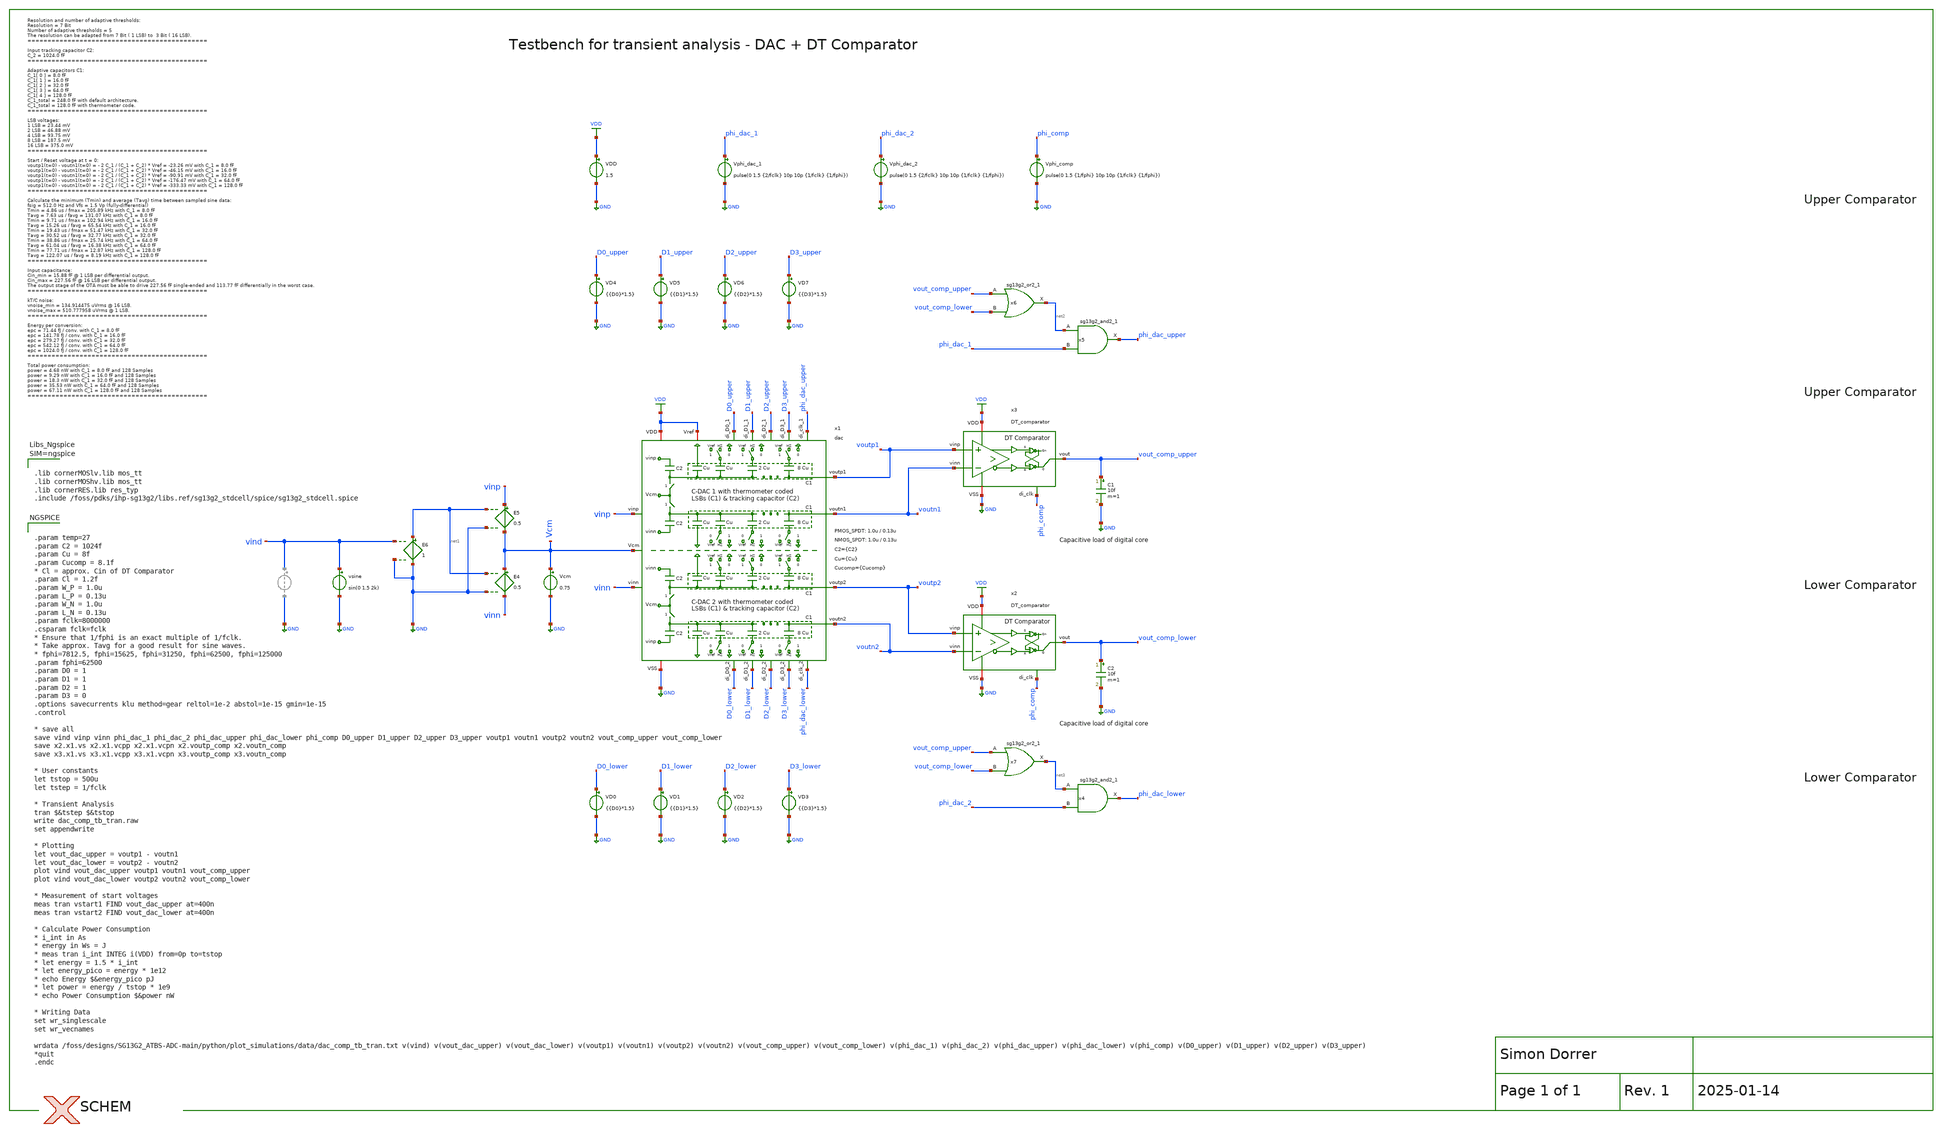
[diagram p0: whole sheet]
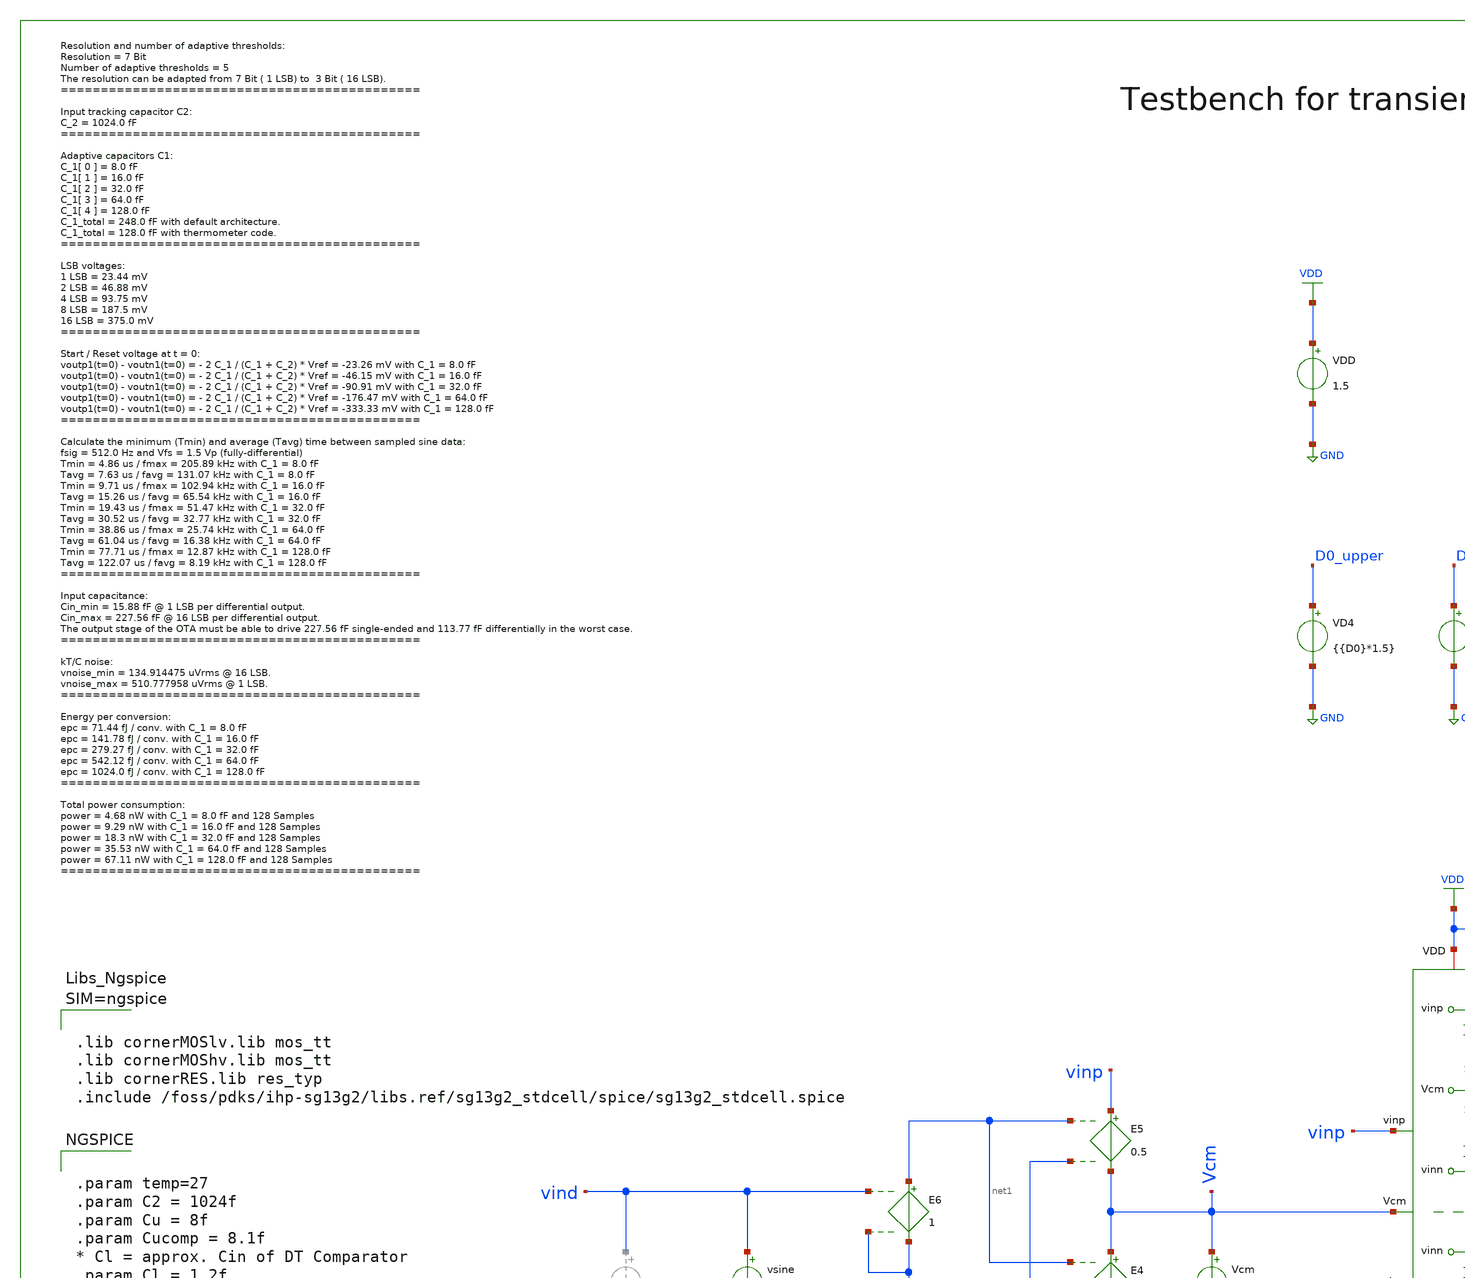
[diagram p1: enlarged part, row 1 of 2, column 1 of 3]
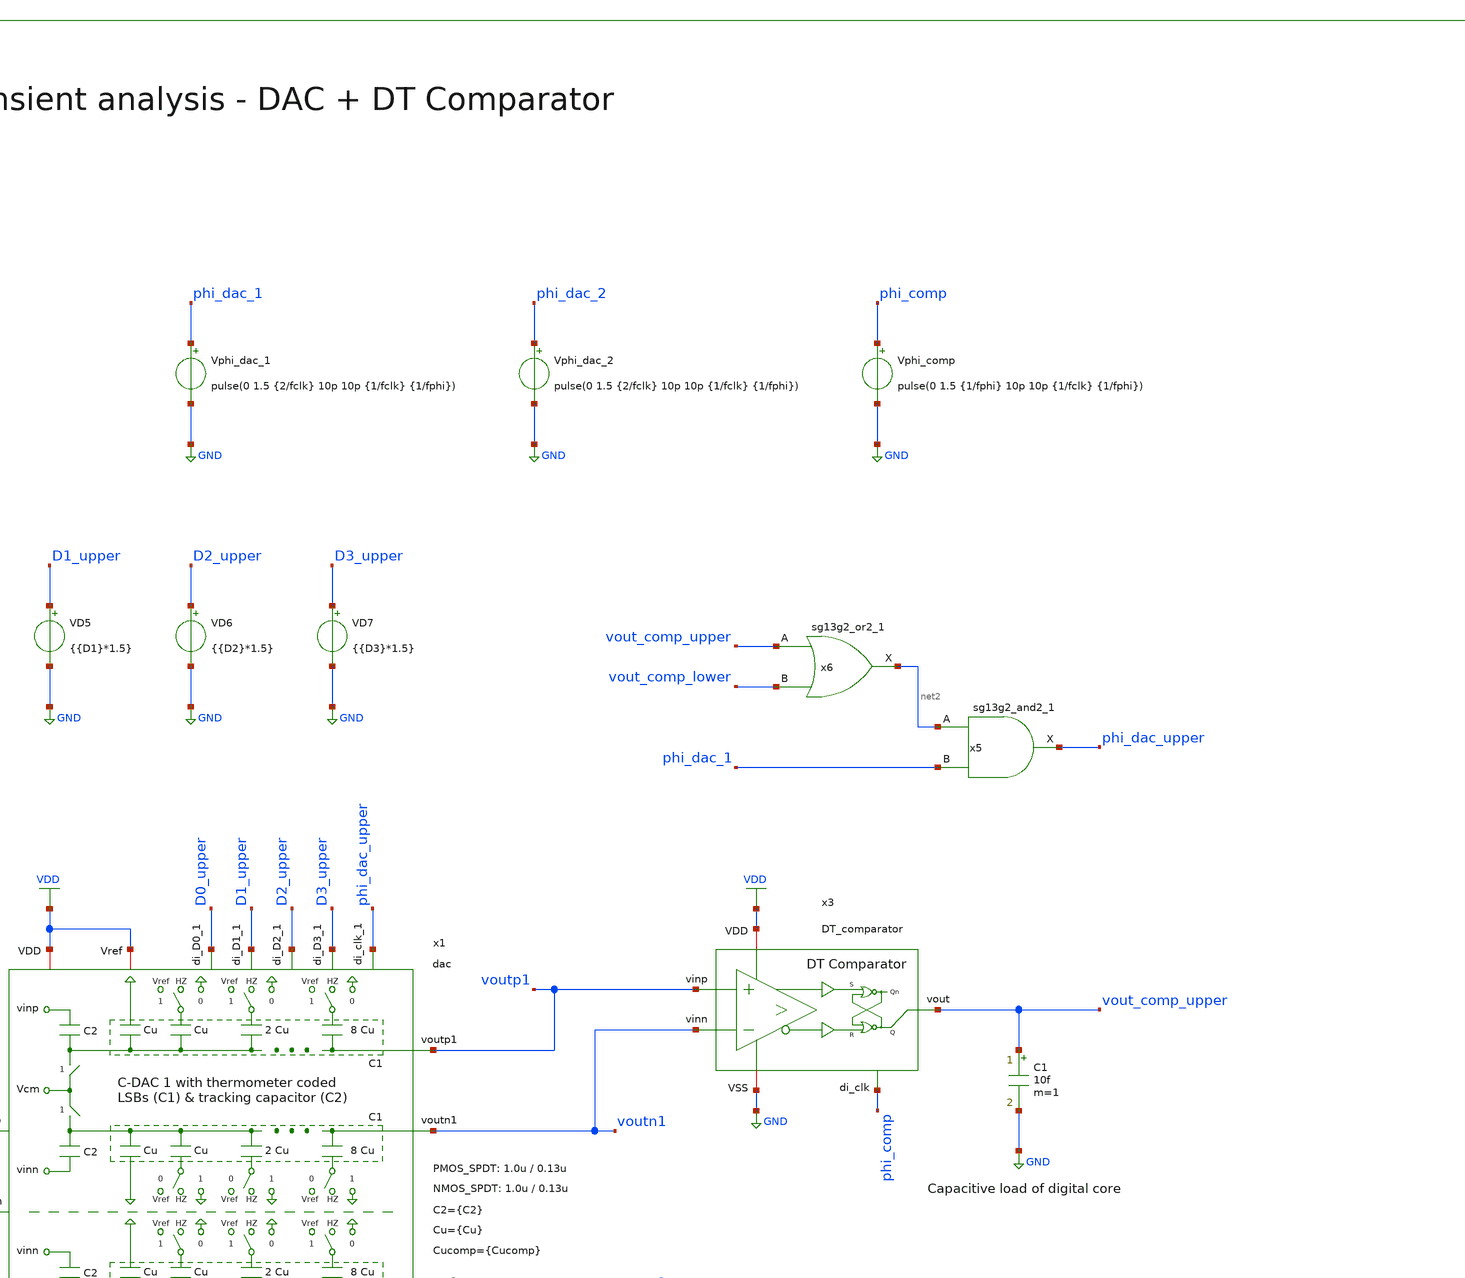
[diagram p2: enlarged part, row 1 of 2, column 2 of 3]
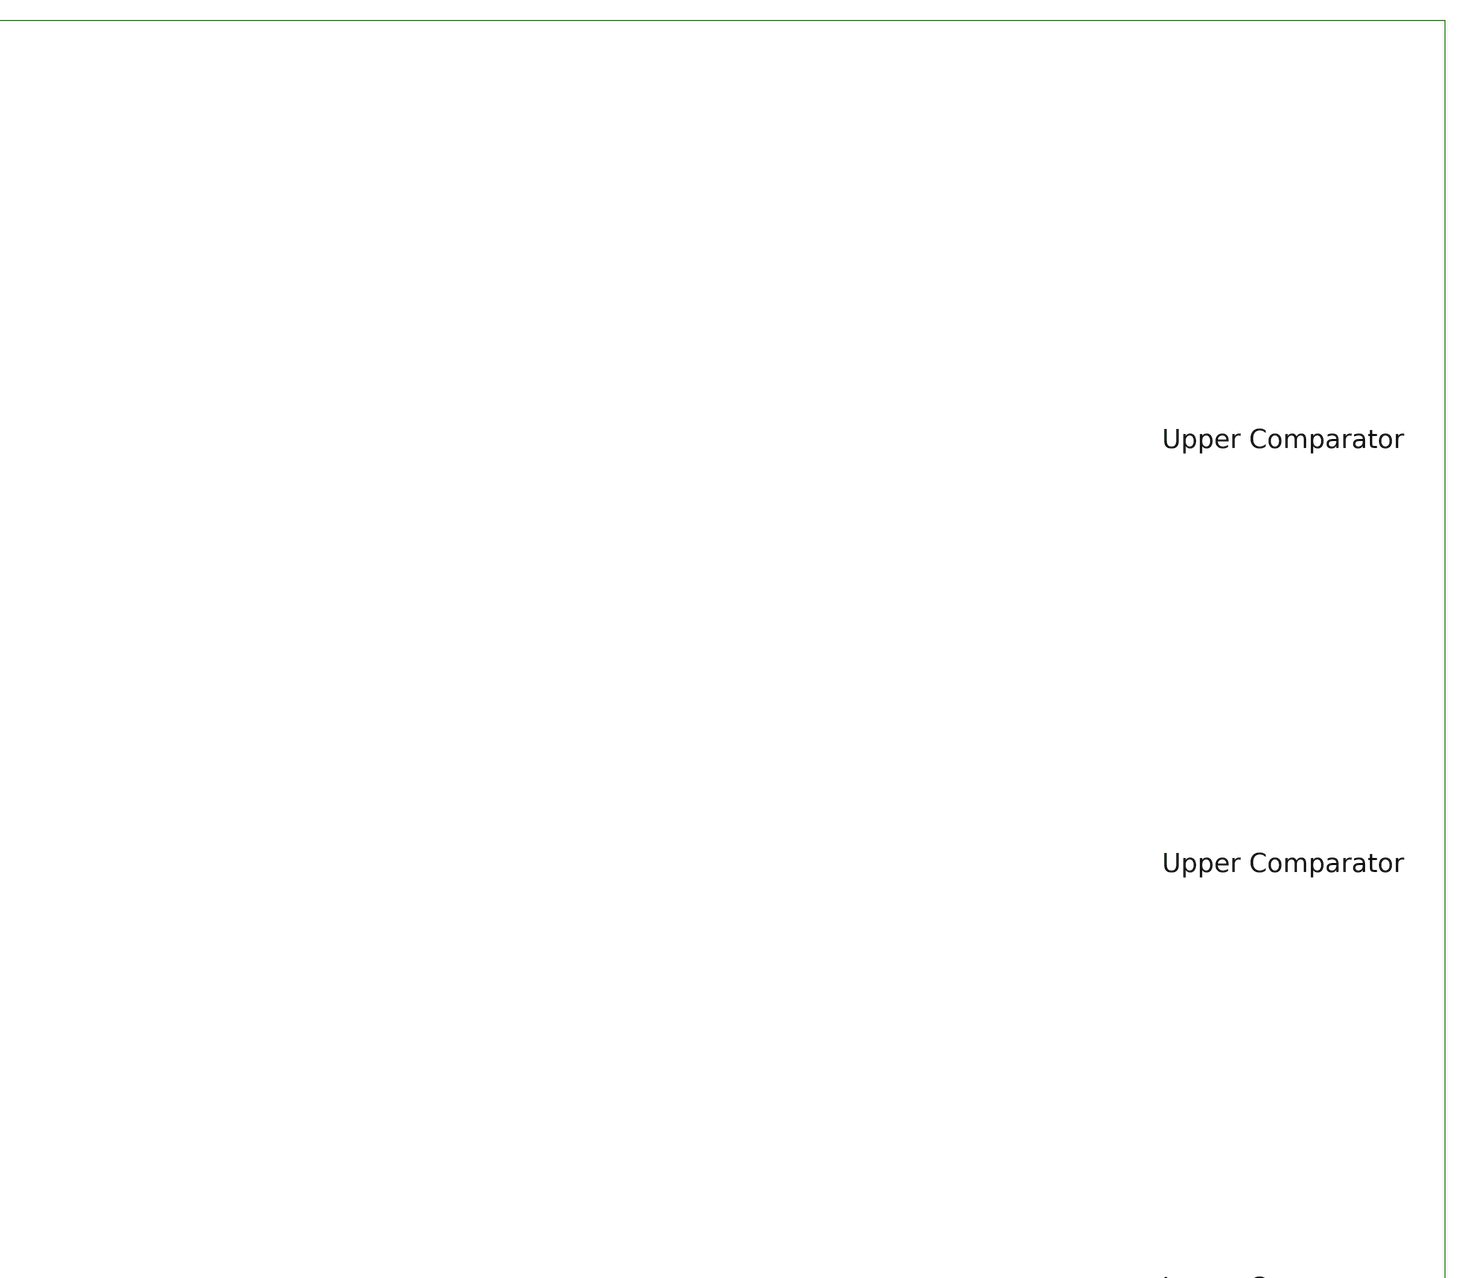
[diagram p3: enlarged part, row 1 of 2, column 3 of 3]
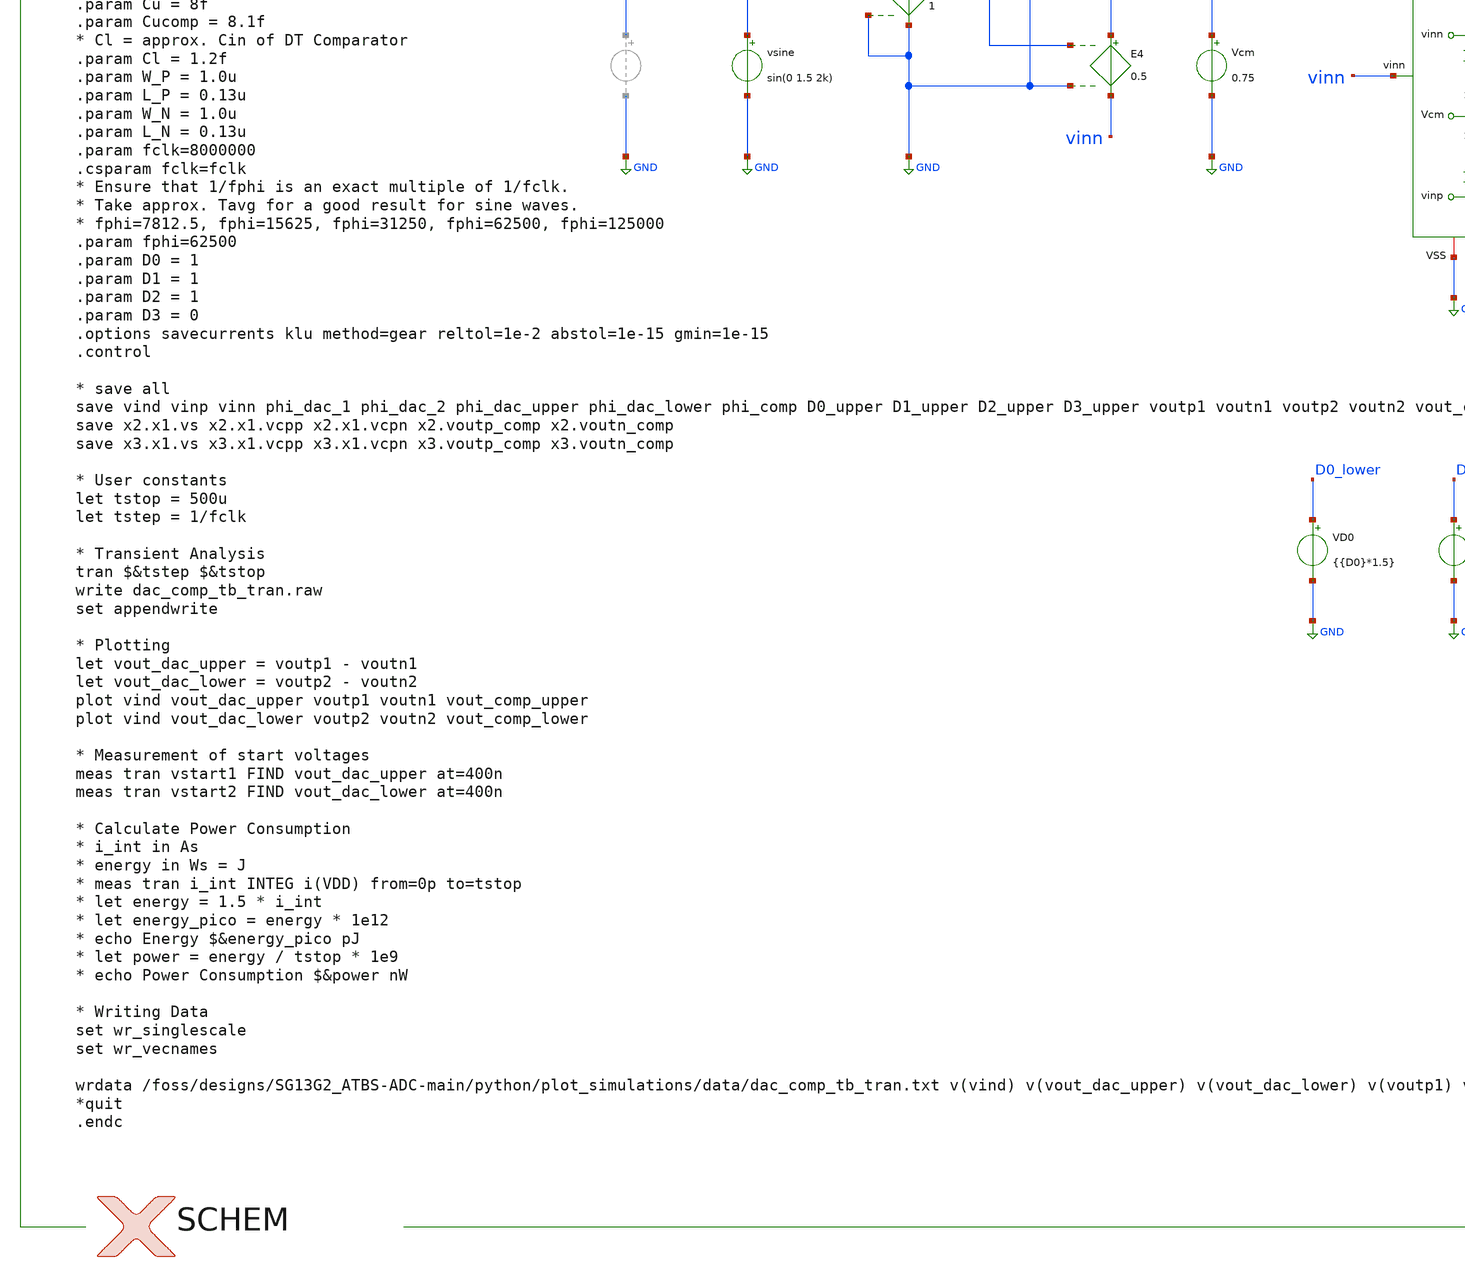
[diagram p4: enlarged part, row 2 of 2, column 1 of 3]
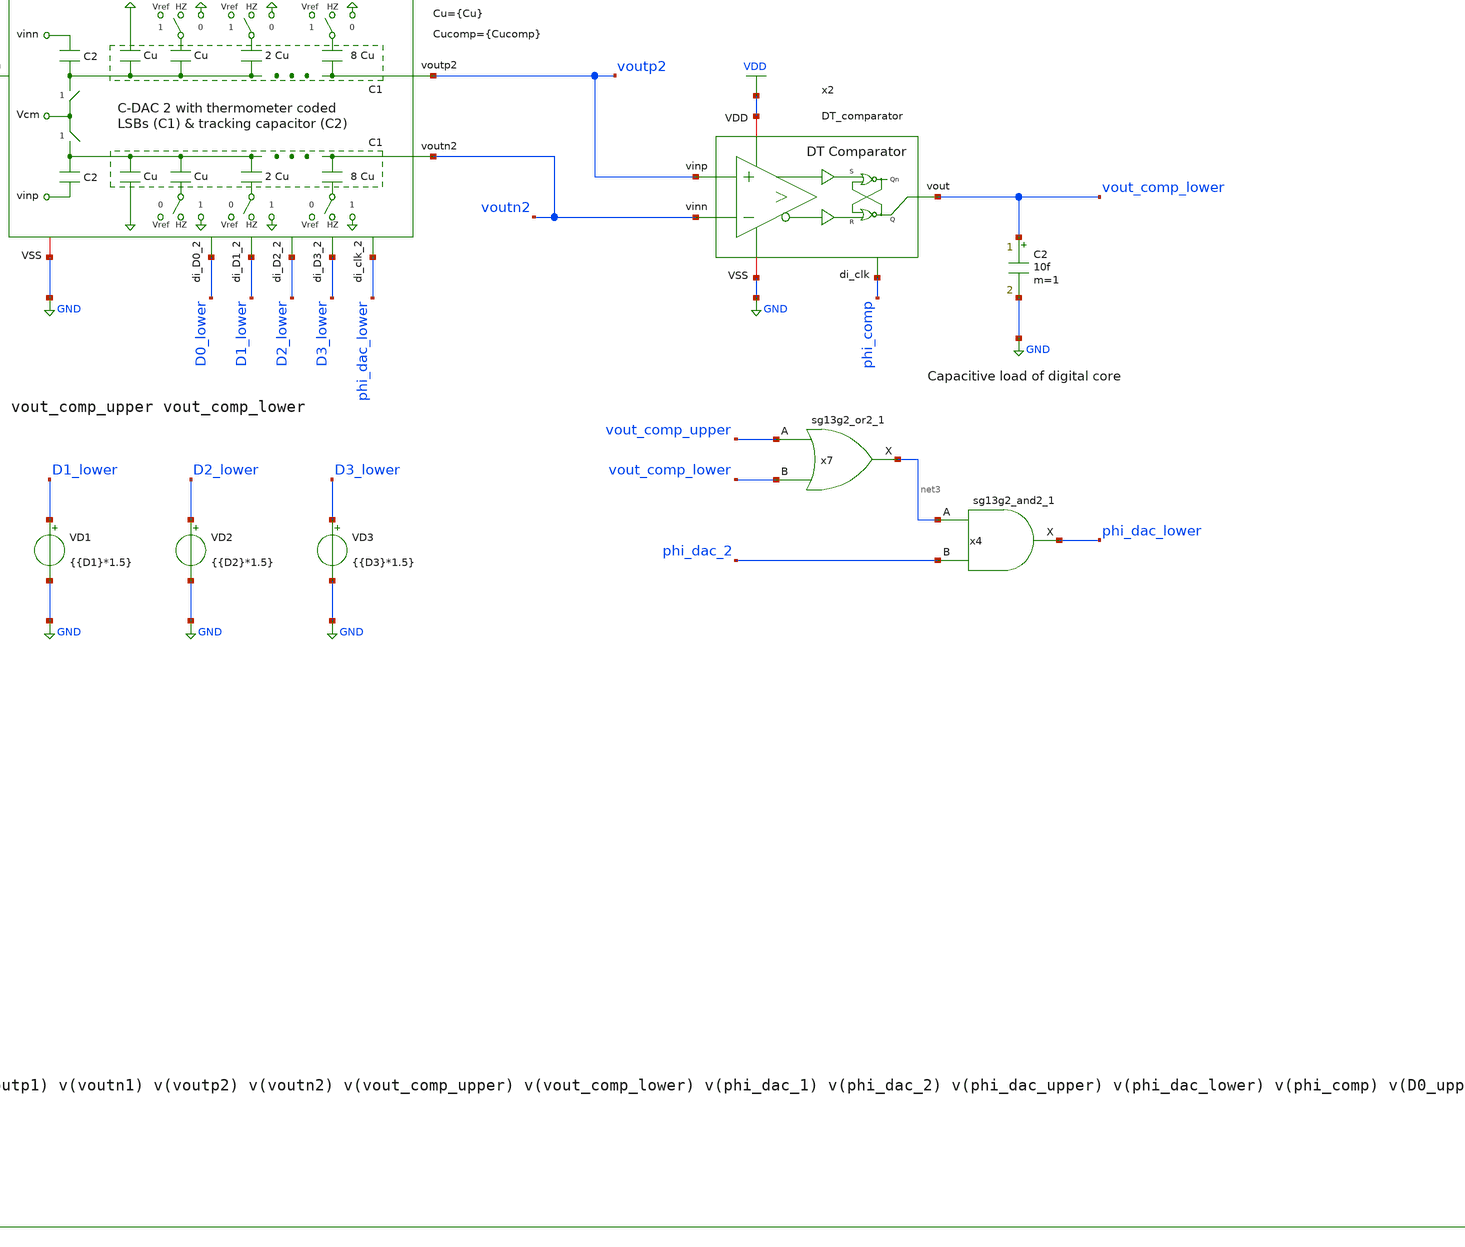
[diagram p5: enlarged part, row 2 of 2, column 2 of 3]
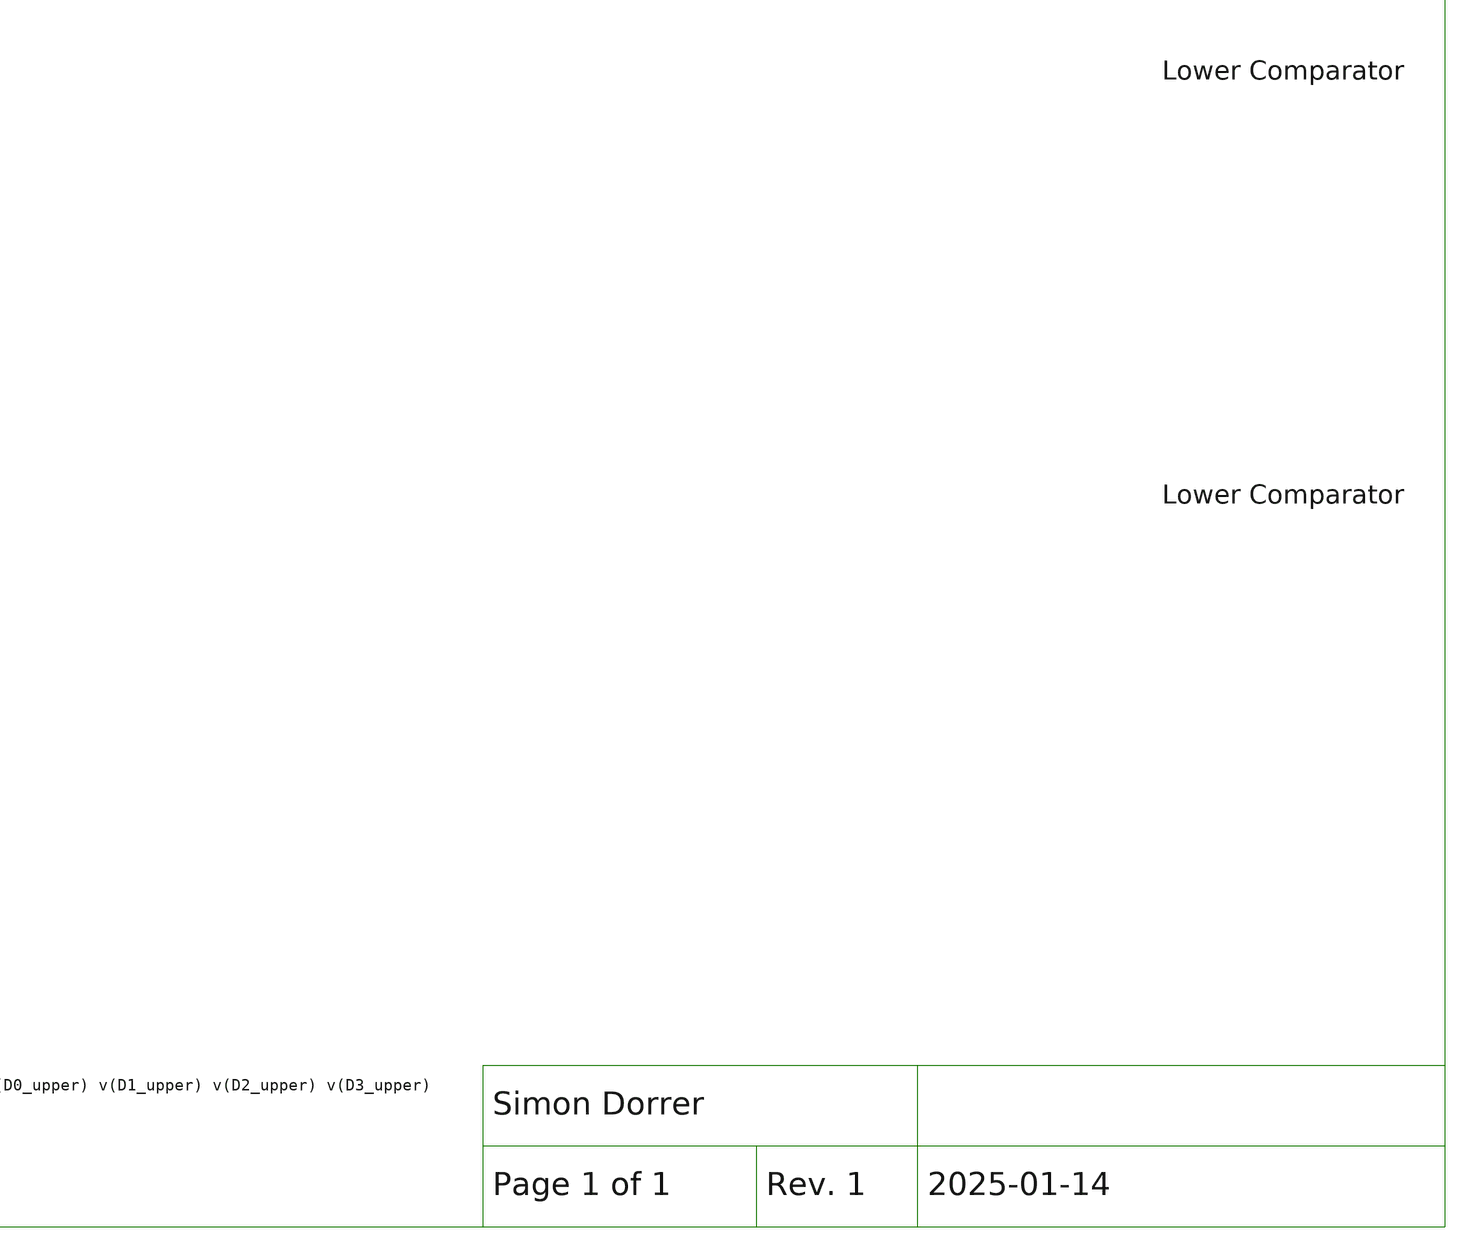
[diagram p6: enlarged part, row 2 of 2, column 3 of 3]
** sch_path: SG13G2_ATBS-ADC-main/xschem/dac/testbenches/dac_comp_tb_tran.sch
**.subckt dac_comp_tb_tran
VDD VDD GND 1.5
Vcm Vcm GND 0.75
E4 Vcm vinn net1 GND 0.5
E5 vinp Vcm net1 GND 0.5
E6 net1 GND vind GND 1
VD0 D0_lower GND {{D0}*1.5}
VD1 D1_lower GND {{D1}*1.5}
VD2 D2_lower GND {{D2}*1.5}
VD3 D3_lower GND {{D3}*1.5}
Vphi_comp phi_comp GND pulse(0 1.5 {1/fphi} 10p 10p {1/fclk} {1/fphi})
Vphi_dac_1 phi_dac_1 GND pulse(0 1.5 {2/fclk} 10p 10p {1/fclk} {1/fphi})
x2 VDD voutp2 vout_comp_lower voutn2 phi_comp GND DT_comparator
x3 VDD voutp1 vout_comp_upper voutn1 phi_comp GND DT_comparator
vsine vind GND sin(0 1.5 2k)
x1 VDD vinp voutp1 voutn1 vinn D0_lower D1_lower D2_lower D3_lower GND VDD Vcm voutp2 voutn2 phi_dac_lower
+ D0_upper D1_upper D2_upper D3_upper phi_dac_upper dac W_P_SPDT=1.0u L_P_SPDT=0.13u W_N_SPDT=1.0u L_N_SPDT=0.13u
+ C2={C2} Cu={Cu} Cucomp={Cucomp}
C1 vout_comp_upper GND 10f m=1
C2 vout_comp_lower GND 10f m=1
x5 phi_dac_upper net2 phi_dac_1 VDD GND sg13g2_and2_1
VD4 D0_upper GND {{D0}*1.5}
VD5 D1_upper GND {{D1}*1.5}
VD6 D2_upper GND {{D2}*1.5}
VD7 D3_upper GND {{D3}*1.5}
x6 net2 vout_comp_upper vout_comp_lower VDD GND sg13g2_or2_1
x4 phi_dac_lower net3 phi_dac_2 VDD GND sg13g2_and2_1
x7 net3 vout_comp_upper vout_comp_lower VDD GND sg13g2_or2_1
Vphi_dac_2 phi_dac_2 GND pulse(0 1.5 {2/fclk} 10p 10p {1/fclk} {1/fphi})
**** begin user architecture code


.param temp=27
.param C2 = 1024f
.param Cu = 8f
.param Cucomp = 8.1f
* Cl = approx. Cin of DT Comparator
.param Cl = 1.2f
.param W_P = 1.0u
.param L_P = 0.13u
.param W_N = 1.0u
.param L_N = 0.13u
.param fclk=8000000
.csparam fclk=fclk
* Ensure that 1/fphi is an exact multiple of 1/fclk.
* Take approx. Tavg for a good result for sine waves.
* fphi=7812.5, fphi=15625, fphi=31250, fphi=62500, fphi=125000
.param fphi=62500
.param D0 = 1
.param D1 = 1
.param D2 = 1
.param D3 = 0
.options savecurrents klu method=gear reltol=1e-2 abstol=1e-15 gmin=1e-15
.control

* save all
save vind vinp vinn phi_dac_1 phi_dac_2 phi_dac_upper phi_dac_lower phi_comp D0_upper D1_upper
+ D2_upper D3_upper voutp1 voutn1 voutp2 voutn2 vout_comp_upper vout_comp_lower
save x2.x1.vs x2.x1.vcpp x2.x1.vcpn x2.voutp_comp x2.voutn_comp
save x3.x1.vs x3.x1.vcpp x3.x1.vcpn x3.voutp_comp x3.voutn_comp

* User constants
let tstop = 500u
let tstep = 1/fclk

* Transient Analysis
tran $&tstep $&tstop
write dac_comp_tb_tran.raw
set appendwrite

* Plotting
let vout_dac_upper = voutp1 - voutn1
let vout_dac_lower = voutp2 - voutn2
plot vind vout_dac_upper voutp1 voutn1 vout_comp_upper
plot vind vout_dac_lower voutp2 voutn2 vout_comp_lower

* Measurement of start voltages
meas tran vstart1 FIND vout_dac_upper at=400n
meas tran vstart2 FIND vout_dac_lower at=400n

* Calculate Power Consumption
* i_int in As
* energy in Ws = J
* meas tran i_int INTEG i(VDD) from=0p to=tstop
* let energy = 1.5 * i_int
* let energy_pico = energy * 1e12
* echo Energy $&energy_pico pJ
* let power = energy / tstop * 1e9
* echo Power Consumption $&power nW

* Writing Data
set wr_singlescale
set wr_vecnames

wrdata /foss/designs/SG13G2_ATBS-ADC-main/python/plot_simulations/data/dac_comp_tb_tran.txt v(vind)
+ v(vout_dac_upper) v(vout_dac_lower) v(voutp1) v(voutn1) v(voutp2) v(voutn2) v(vout_comp_upper) v(vout_comp_lower)
+ v(phi_dac_1) v(phi_dac_2) v(phi_dac_upper) v(phi_dac_lower) v(phi_comp) v(D0_upper) v(D1_upper) v(D2_upper)
+ v(D3_upper)
*quit
.endc





.lib cornerMOSlv.lib mos_tt
.lib cornerMOShv.lib mos_tt
.lib cornerRES.lib res_typ
.include /foss/pdks/ihp-sg13g2/libs.ref/sg13g2_stdcell/spice/sg13g2_stdcell.spice



**** end user architecture code
**.ends

* expanding   symbol:  comparator/discrete_time/DT_comparator.sym # of pins=6
** sym_path: SG13G2_ATBS-ADC-main/xschem/comparator/discrete_time/DT_comparator.sym
** sch_path: SG13G2_ATBS-ADC-main/xschem/comparator/discrete_time/DT_comparator.sch
.subckt DT_comparator VDD vinp vout vinn di_clk VSS
*.iopin VDD
*.opin vout
*.iopin VSS
*.ipin vinp
*.ipin vinn
*.ipin di_clk
x2 VDD voutp_comp voutp_buf VSS buffer_lv W_P_INV=1.0u L_P_INV=0.13u W_N_INV=1.0u L_N_INV=0.13u
x3 VDD voutn_comp voutn_buf VSS buffer_lv W_P_INV=1.0u L_P_INV=0.13u W_N_INV=1.0u L_N_INV=0.13u
x5 VDD di_clk net1 VSS inverter_lv W_P=1.0u L_P=0.13u W_N=1.0u L_N=0.13u
* noconn #net2
x4 VDD voutp_buf net2 VSS vout voutn_buf SR_latch W_P_SR=1.0u L_P_SR=0.13u W_N_SR=1.0u L_N_SR=0.13u
x1 net1 di_clk VDD voutp_comp vinp VSS voutn_comp vinn dynamic_biasing_comparator
.ends


* expanding   symbol:  dac/dac.sym # of pins=20
** sym_path: SG13G2_ATBS-ADC-main/xschem/dac/dac.sym
** sch_path: SG13G2_ATBS-ADC-main/xschem/dac/dac.sch
.subckt dac VDD vinp voutp1 voutn1 vinn di_D0_2 di_D1_2 di_D2_2 di_D3_2 VSS Vref Vcm voutp2 voutn2
+ di_clk_2 di_D0_1 di_D1_1 di_D2_1 di_D3_1 di_clk_1  W_P_SPDT=1.0u L_P_SPDT=0.13u W_N_SPDT=1.0u L_N_SPDT=0.13u
+ C2=1024f Cu=8f Cucomp=8.1f
*.opin voutp1
*.ipin di_D0_1
*.iopin VSS
*.iopin Vref
*.opin voutn1
*.ipin vinp
*.ipin vinn
*.ipin di_D1_1
*.ipin di_D2_1
*.ipin di_D3_1
*.opin voutp2
*.opin voutn2
*.iopin VDD
*.ipin Vcm
*.ipin di_clk_1
*.ipin di_D3_2
*.ipin di_D2_2
*.ipin di_D1_2
*.ipin di_D0_2
*.ipin di_clk_2
C2a vinp voutp1 C2 m=1
C2b vinn voutn1 C2 m=1
C1a net3 voutp1 Cucomp m=1
C1b net1 voutn1 Cucomp m=1
x2 VDD di_clk_1 VSS voutp1 Vcm clk_1_n transmission_gate_lv_wo_dummy W_P=1.0u L_P=0.13u W_N=1.0u
+ L_N=0.13u
x3 VDD di_clk_1 VSS voutn1 Vcm clk_1_n transmission_gate_lv_wo_dummy W_P=1.0u L_P=0.13u W_N=1.0u
+ L_N=0.13u
x1 VDD di_clk_1 clk_1_n VSS inverter_lv W_P=W_P_SPDT L_P=L_P_SPDT W_N=W_N_SPDT L_N=L_N_SPDT
x5 Vref VSS VSS di_D1_1 di_clk_1 VDD voutp1 unit_cell W_P_SPDT=W_P_SPDT L_P_SPDT=L_P_SPDT
+ W_N_SPDT=W_N_SPDT L_N_SPDT=L_N_SPDT Cu=2*Cu
x6 Vref VSS VSS di_D2_1 di_clk_1 VDD voutp1 unit_cell W_P_SPDT=W_P_SPDT L_P_SPDT=L_P_SPDT
+ W_N_SPDT=W_N_SPDT L_N_SPDT=L_N_SPDT Cu=4*Cu
x4 Vref VSS VSS di_D0_1 di_clk_1 VDD voutp1 unit_cell W_P_SPDT=W_P_SPDT L_P_SPDT=L_P_SPDT
+ W_N_SPDT=W_N_SPDT L_N_SPDT=L_N_SPDT Cu=Cu
x7 Vref VSS VSS di_D3_1 di_clk_1 VDD voutp1 unit_cell W_P_SPDT=W_P_SPDT L_P_SPDT=L_P_SPDT
+ W_N_SPDT=W_N_SPDT L_N_SPDT=L_N_SPDT Cu=8*Cu
x9 VSS Vref VSS di_D0_1 di_clk_1 VDD voutn1 unit_cell W_P_SPDT=W_P_SPDT L_P_SPDT=L_P_SPDT
+ W_N_SPDT=W_N_SPDT L_N_SPDT=L_N_SPDT Cu=Cu
x10 VSS Vref VSS di_D1_1 di_clk_1 VDD voutn1 unit_cell W_P_SPDT=W_P_SPDT L_P_SPDT=L_P_SPDT
+ W_N_SPDT=W_N_SPDT L_N_SPDT=L_N_SPDT Cu=2*Cu
x11 VSS Vref VSS di_D2_1 di_clk_1 VDD voutn1 unit_cell W_P_SPDT=W_P_SPDT L_P_SPDT=L_P_SPDT
+ W_N_SPDT=W_N_SPDT L_N_SPDT=L_N_SPDT Cu=4*Cu
x12 VSS Vref VSS di_D3_1 di_clk_1 VDD voutn1 unit_cell W_P_SPDT=W_P_SPDT L_P_SPDT=L_P_SPDT
+ W_N_SPDT=W_N_SPDT L_N_SPDT=L_N_SPDT Cu=8*Cu
C1 vinn voutp2 C2 m=1
C2 vinp voutn2 C2 m=1
C1c net2 voutp2 Cucomp m=1
C1d net4 voutn2 Cucomp m=1
x14 VDD di_clk_2 VSS voutp2 Vcm clk_2_n transmission_gate_lv_wo_dummy W_P=1.0u L_P=0.13u W_N=1.0u
+ L_N=0.13u
x15 VDD di_clk_2 VSS voutn2 Vcm clk_2_n transmission_gate_lv_wo_dummy W_P=1.0u L_P=0.13u W_N=1.0u
+ L_N=0.13u
x17 Vref VSS VSS di_D1_2 di_clk_2 VDD voutp2 unit_cell W_P_SPDT=W_P_SPDT L_P_SPDT=L_P_SPDT
+ W_N_SPDT=W_N_SPDT L_N_SPDT=L_N_SPDT Cu=2*Cu
x18 Vref VSS VSS di_D2_2 di_clk_2 VDD voutp2 unit_cell W_P_SPDT=W_P_SPDT L_P_SPDT=L_P_SPDT
+ W_N_SPDT=W_N_SPDT L_N_SPDT=L_N_SPDT Cu=4*Cu
x16 Vref VSS VSS di_D0_2 di_clk_2 VDD voutp2 unit_cell W_P_SPDT=W_P_SPDT L_P_SPDT=L_P_SPDT
+ W_N_SPDT=W_N_SPDT L_N_SPDT=L_N_SPDT Cu=Cu
x19 Vref VSS VSS di_D3_2 di_clk_2 VDD voutp2 unit_cell W_P_SPDT=W_P_SPDT L_P_SPDT=L_P_SPDT
+ W_N_SPDT=W_N_SPDT L_N_SPDT=L_N_SPDT Cu=8*Cu
x21 VSS Vref VSS di_D0_2 di_clk_2 VDD voutn2 unit_cell W_P_SPDT=W_P_SPDT L_P_SPDT=L_P_SPDT
+ W_N_SPDT=W_N_SPDT L_N_SPDT=L_N_SPDT Cu=Cu
x22 VSS Vref VSS di_D1_2 di_clk_2 VDD voutn2 unit_cell W_P_SPDT=W_P_SPDT L_P_SPDT=L_P_SPDT
+ W_N_SPDT=W_N_SPDT L_N_SPDT=L_N_SPDT Cu=2*Cu
x23 VSS Vref VSS di_D2_2 di_clk_2 VDD voutn2 unit_cell W_P_SPDT=W_P_SPDT L_P_SPDT=L_P_SPDT
+ W_N_SPDT=W_N_SPDT L_N_SPDT=L_N_SPDT Cu=4*Cu
x24 VSS Vref VSS di_D3_2 di_clk_2 VDD voutn2 unit_cell W_P_SPDT=W_P_SPDT L_P_SPDT=L_P_SPDT
+ W_N_SPDT=W_N_SPDT L_N_SPDT=L_N_SPDT Cu=8*Cu
x8 VDD di_clk_1 VSS net3 VSS Vref spdt_switch W_P_TG=W_P_SPDT L_P_TG=L_P_SPDT W_N_TG=W_N_SPDT
+ L_N_TG=L_N_SPDT
x13 VDD di_clk_1 VSS net1 Vref VSS spdt_switch W_P_TG=W_P_SPDT L_P_TG=L_P_SPDT W_N_TG=W_N_SPDT
+ L_N_TG=L_N_SPDT
x20 VDD di_clk_2 VSS net2 VSS Vref spdt_switch W_P_TG=W_P_SPDT L_P_TG=L_P_SPDT W_N_TG=W_N_SPDT
+ L_N_TG=L_N_SPDT
x25 VDD di_clk_2 VSS net4 Vref VSS spdt_switch W_P_TG=W_P_SPDT L_P_TG=L_P_SPDT W_N_TG=W_N_SPDT
+ L_N_TG=L_N_SPDT
x26 VDD di_clk_2 clk_2_n VSS inverter_lv W_P=W_P_SPDT L_P=L_P_SPDT W_N=W_N_SPDT L_N=L_N_SPDT
.ends


* expanding   symbol:  sg13g2_stdcells/sg13g2_and2_1.sym # of pins=3
** sym_path: sg13g2_stdcells/sg13g2_and2_1.sym
** sch_path: sg13g2_stdcells/sg13g2_and2_1.sch
.subckt sg13g2_and2_1 X A B VDD VSS
*.ipin A
*.ipin B
*.opin X
*.iopin VDD
*.iopin VSS
XM1 net1 A net2 VSS sg13_lv_nmos w=640.00n l=130.00n ng=1 m=1 mm_ok=1
XM2 net2 B VSS VSS sg13_lv_nmos w=640.00n l=130.00n ng=1 m=1 mm_ok=1
XM3 X net1 VSS VSS sg13_lv_nmos w=740.00n l=130.00n ng=1 m=1 mm_ok=1
XM4 net1 B VDD VDD sg13_lv_pmos w=840.00n l=130.00n ng=1 m=1 mm_ok=1
XM5 net1 A VDD VDD sg13_lv_pmos w=840.00n l=130.00n ng=1 m=1 mm_ok=1
XM6 X net1 VDD VDD sg13_lv_pmos w=1.12u l=130.00n ng=1 m=1 mm_ok=1
.ends


* expanding   symbol:  sg13g2_stdcells/sg13g2_or2_1.sym # of pins=3
** sym_path: sg13g2_stdcells/sg13g2_or2_1.sym
** sch_path: sg13g2_stdcells/sg13g2_or2_1.sch
.subckt sg13g2_or2_1 X A B VDD VSS
*.opin X
*.ipin B
*.ipin A
*.iopin VDD
*.iopin VSS
XM1 net1 B VSS VSS sg13_lv_nmos w=550.00n l=130.00n ng=1 m=1 mm_ok=1
XM2 net1 A VSS VSS sg13_lv_nmos w=550.00n l=130.00n ng=1 m=1 mm_ok=1
XM3 X net1 VSS VSS sg13_lv_nmos w=740.00n l=130.00n ng=1 m=1 mm_ok=1
XM4 net2 A VDD VDD sg13_lv_pmos w=840.00n l=130.00n ng=1 m=1 mm_ok=1
XM5 net1 B net2 VDD sg13_lv_pmos w=840.00n l=130.00n ng=1 m=1 mm_ok=1
XM6 X net1 VDD VDD sg13_lv_pmos w=1.12u l=130.00n ng=1 m=1 mm_ok=1
.ends


* expanding   symbol:  buffer/buffer_lv.sym # of pins=4
** sym_path: SG13G2_ATBS-ADC-main/xschem/buffer/buffer_lv.sym
** sch_path: SG13G2_ATBS-ADC-main/xschem/buffer/buffer_lv.sch
.subckt buffer_lv VDD vin vout VSS  W_P_INV=3.0u L_P_INV=0.13u W_N_INV=1.0u L_N_INV=0.13u
*.ipin vin
*.iopin VDD
*.iopin VSS
*.opin vout
x1 VDD vin net1 VSS inverter_lv W_P=W_P_INV L_P=L_P_INV W_N=W_N_INV L_N=L_N_INV
x2 VDD net1 vout VSS inverter_lv W_P=W_P_INV L_P=L_P_INV W_N=W_N_INV L_N=L_N_INV
.ends


* expanding   symbol:  inverter/inverter_lv.sym # of pins=4
** sym_path: SG13G2_ATBS-ADC-main/xschem/inverter/inverter_lv.sym
** sch_path: SG13G2_ATBS-ADC-main/xschem/inverter/inverter_lv.sch
.subckt inverter_lv VDD vin vout VSS  W_P=3.0u L_P=0.13u W_N=1.0u L_N=0.13u
*.ipin vin
*.iopin VDD
*.iopin VSS
*.opin vout
XM1 vout vin VDD VDD sg13_lv_pmos w=W_P l=L_P ng=1 m=1 mm_ok=1
XM2 vout vin VSS VSS sg13_lv_nmos w=W_N l=L_N ng=1 m=1 mm_ok=1
.ends


* expanding   symbol:  comparator/SR_latch/SR_latch.sym # of pins=6
** sym_path: SG13G2_ATBS-ADC-main/xschem/comparator/SR_latch/SR_latch.sym
** sch_path: SG13G2_ATBS-ADC-main/xschem/comparator/SR_latch/SR_latch.sch
.subckt SR_latch VDD S Qn VSS Q R  W_P_SR=1.0u L_P_SR=0.13u W_N_SR=1.0u L_N_SR=0.13u
*.iopin VDD
*.opin Q
*.iopin VSS
*.ipin S
*.ipin R
*.opin Qn
x1 VDD Q R Qn VSS NOR_gate W_P=W_P_SR L_P=L_P_SR W_N=W_N_SR L_N=L_N_SR
x2 VDD Qn Q S VSS NOR_gate W_P=W_P_SR L_P=L_P_SR W_N=W_N_SR L_N=L_N_SR
.ends


* expanding   symbol:  comparator/discrete_time/Dynamic-biasing/dynamic_biasing_comparator.sym # of
*+ pins=8
** sym_path: SG13G2_ATBS-ADC-main/xschem/comparator/discrete_time/Dynamic-biasing/dynamic_biasing_comparator.sym
** sch_path: SG13G2_ATBS-ADC-main/xschem/comparator/discrete_time/Dynamic-biasing/dynamic_biasing_comparator.sch
.subckt dynamic_biasing_comparator di_clk_n di_clk VDD voutp vinp VSS voutn vinn
*.iopin VDD
*.opin voutp
*.opin voutn
*.ipin di_clk_n
*.iopin VSS
*.ipin vinp
*.ipin vinn
*.ipin di_clk
XM3a vs di_clk vctail VSS sg13_lv_nmos w=1.0u l=0.13u ng=1 m=1 mm_ok=1
XM12 voutp di_clk_n VSS VSS sg13_lv_nmos w=1.0u l=0.13u ng=1 m=1 mm_ok=1
XM8 net1 voutn VDD VDD sg13_lv_pmos w=2.0u l=0.13u ng=2 m=1 mm_ok=1
XM10 voutp voutn VSS VSS sg13_lv_nmos w=1.0u l=0.13u ng=1 m=1 mm_ok=1
XM11 voutn voutp VSS VSS sg13_lv_nmos w=1.0u l=0.13u ng=1 m=1 mm_ok=1
XM13 voutn di_clk_n VSS VSS sg13_lv_nmos w=1.0u l=0.13u ng=1 m=1 mm_ok=1
CPn vcpn VSS 300f m=1
CPp vcpp VSS 300f m=1
XM9 net2 voutp VDD VDD sg13_lv_pmos w=2.0u l=0.13u ng=2 m=1 mm_ok=1
XM6 voutp vcpn net1 VDD sg13_lv_pmos w=2.0u l=0.13u ng=2 m=1 mm_ok=1
XM7 voutn vcpp net2 VDD sg13_lv_pmos w=2.0u l=0.13u ng=2 m=1 mm_ok=1
CTAIL vctail VSS 600f m=1
XM3b vctail di_clk_n VSS VSS sg13_lv_nmos w=1.0u l=0.13u ng=1 m=1 mm_ok=1
XM1 vcpn vinp vs VSS sg13_lv_nmos w=1.0u l=0.13u ng=1 m=1 mm_ok=1
XM2 vcpp vinn vs VSS sg13_lv_nmos w=1.0u l=0.13u ng=1 m=1 mm_ok=1
XM4 vcpn di_clk VDD VDD sg13_lv_pmos w=1.0u l=0.13u ng=1 m=1 mm_ok=1
XM5 vcpp di_clk VDD VDD sg13_lv_pmos w=1.0u l=0.13u ng=1 m=1 mm_ok=1
.ends


* expanding   symbol:  transmission_gate/transmission_gate_lv_wo_dummy.sym # of pins=6
** sym_path: SG13G2_ATBS-ADC-main/xschem/transmission_gate/transmission_gate_lv_wo_dummy.sym
** sch_path: SG13G2_ATBS-ADC-main/xschem/transmission_gate/transmission_gate_lv_wo_dummy.sch
.subckt transmission_gate_lv_wo_dummy VDD di_tg_ctrl VSS v_b v_a di_tg_ctrl_n  W_P=1.0u L_P=0.13u
+ W_N=1.0u L_N=0.13u
*.iopin v_a
*.iopin v_b
*.iopin VDD
*.iopin VSS
*.ipin di_tg_ctrl
*.ipin di_tg_ctrl_n
XM1 v_a di_tg_ctrl v_b VSS sg13_lv_nmos w=W_N l=L_N ng=1 m=1 mm_ok=1
XM2 v_a di_tg_ctrl_n v_b VDD sg13_lv_pmos w=W_P l=L_P ng=1 m=1 mm_ok=1
.ends


* expanding   symbol:  dac/unit_cell.sym # of pins=7
** sym_path: SG13G2_ATBS-ADC-main/xschem/dac/unit_cell.sym
** sch_path: SG13G2_ATBS-ADC-main/xschem/dac/unit_cell.sch
.subckt unit_cell v1 v0 VSS di_cell_en di_clk VDD vtop  W_P_SPDT=1.0u L_P_SPDT=0.13u W_N_SPDT=1.0u
+ L_N_SPDT=0.13u Cu=8f
*.ipin di_cell_en
*.iopin VSS
*.iopin v0
*.iopin VDD
*.ipin di_clk
*.iopin v1
*.iopin vtop
x1 VDD di_clk VSS net1 v0 v1 di_cell_en_n spdt_hz_switch W_P_TG=W_P_SPDT L_P_TG=L_P_SPDT
+ W_N_TG=W_N_SPDT L_N_TG=L_N_SPDT
C1 net1 vtop Cu m=1
x3 VDD di_cell_en di_cell_en_n VSS inverter_lv W_P=W_P_SPDT L_P=W_P_SPDT W_N=W_N_SPDT L_N=W_N_SPDT
.ends


* expanding   symbol:  spdt_switch/spdt_switch.sym # of pins=6
** sym_path: SG13G2_ATBS-ADC-main/xschem/spdt_switch/spdt_switch.sym
** sch_path: SG13G2_ATBS-ADC-main/xschem/spdt_switch/spdt_switch.sch
.subckt spdt_switch VDD di_spdt_ctrl VSS v_c v_b v_a  W_P_TG=3.0u L_P_TG=0.13u W_N_TG=1.0u
+ L_N_TG=0.13u
*.iopin v_a
*.iopin v_b
*.iopin v_c
*.iopin VDD
*.iopin VSS
*.ipin di_spdt_ctrl
x1 VDD di_spdt_ctrl VSS v_c v_a di_spdt_ctrl_n transmission_gate_lv_wo_dummy W_P=W_P_TG L_P=L_P_TG
+ W_N=W_N_TG L_N=L_N_TG
x2 VDD di_spdt_ctrl_n VSS v_b v_c di_spdt_ctrl transmission_gate_lv_wo_dummy W_P=W_P_TG L_P=L_P_TG
+ W_N=W_N_TG L_N=L_N_TG
x8 VDD di_spdt_ctrl di_spdt_ctrl_n VSS inverter_lv W_P=W_P_TG L_P=L_P_TG W_N=W_N_TG L_N=L_N_TG
.ends


* expanding   symbol:  comparator/NOR_gate/NOR_gate.sym # of pins=5
** sym_path: SG13G2_ATBS-ADC-main/xschem/comparator/NOR_gate/NOR_gate.sym
** sch_path: SG13G2_ATBS-ADC-main/xschem/comparator/NOR_gate/NOR_gate.sch
.subckt NOR_gate VDD C A B VSS  W_P=1.0u L_P=0.13u W_N=0.5u L_N=0.13u
*.iopin VDD
*.opin C
*.iopin VSS
*.ipin A
*.ipin B
XM1 C A VSS VSS sg13_lv_nmos w=W_N l=L_N ng=1 m=1 mm_ok=1
XM2 C B VSS VSS sg13_lv_nmos w=W_N l=L_N ng=1 m=1 mm_ok=1
XM3 C B net1 VDD sg13_lv_pmos w=W_P l=L_P ng=1 m=1 mm_ok=1
XM4 net1 A VDD VDD sg13_lv_pmos w=W_P l=L_P ng=1 m=1 mm_ok=1
XM5 C A net2 VDD sg13_lv_pmos w=W_P l=L_P ng=1 m=1 mm_ok=1
XM6 net2 B VDD VDD sg13_lv_pmos w=W_P l=L_P ng=1 m=1 mm_ok=1
.ends


* expanding   symbol:  spdt_switch/spdt_hz_switch.sym # of pins=7
** sym_path: SG13G2_ATBS-ADC-main/xschem/spdt_switch/spdt_hz_switch.sym
** sch_path: SG13G2_ATBS-ADC-main/xschem/spdt_switch/spdt_hz_switch.sch
.subckt spdt_hz_switch VDD di_spdt_ctrl VSS v_c v_b v_a di_spdt_hz  W_P_TG=3.0u L_P_TG=0.13u
+ W_N_TG=1.0u L_N_TG=0.13u
*.iopin v_a
*.iopin v_b
*.iopin v_c
*.iopin VDD
*.iopin VSS
*.ipin di_spdt_ctrl
*.ipin di_spdt_hz
x1 VDD di_spdt_ctrl VSS net1 v_a di_spdt_ctrl_n transmission_gate_lv_wo_dummy W_P=W_P_TG L_P=L_P_TG
+ W_N=W_N_TG L_N=L_N_TG
x2 VDD di_spdt_ctrl_n VSS v_b net1 di_spdt_ctrl transmission_gate_lv_wo_dummy W_P=W_P_TG L_P=L_P_TG
+ W_N=W_N_TG L_N=L_N_TG
x8 VDD di_spdt_ctrl di_spdt_ctrl_n VSS inverter_lv W_P=W_P_TG L_P=L_P_TG W_N=W_N_TG L_N=L_N_TG
x3 VDD di_spdt_hz di_spdt_hz_n VSS inverter_lv W_P=W_P_TG L_P=L_P_TG W_N=W_N_TG L_N=L_N_TG
x4 VDD di_spdt_hz_n VSS v_c net1 di_spdt_hz transmission_gate_lv_wo_dummy W_P=W_P_TG L_P=L_P_TG
+ W_N=W_N_TG L_N=L_N_TG
.ends

.GLOBAL GND
.GLOBAL VDD
.end
